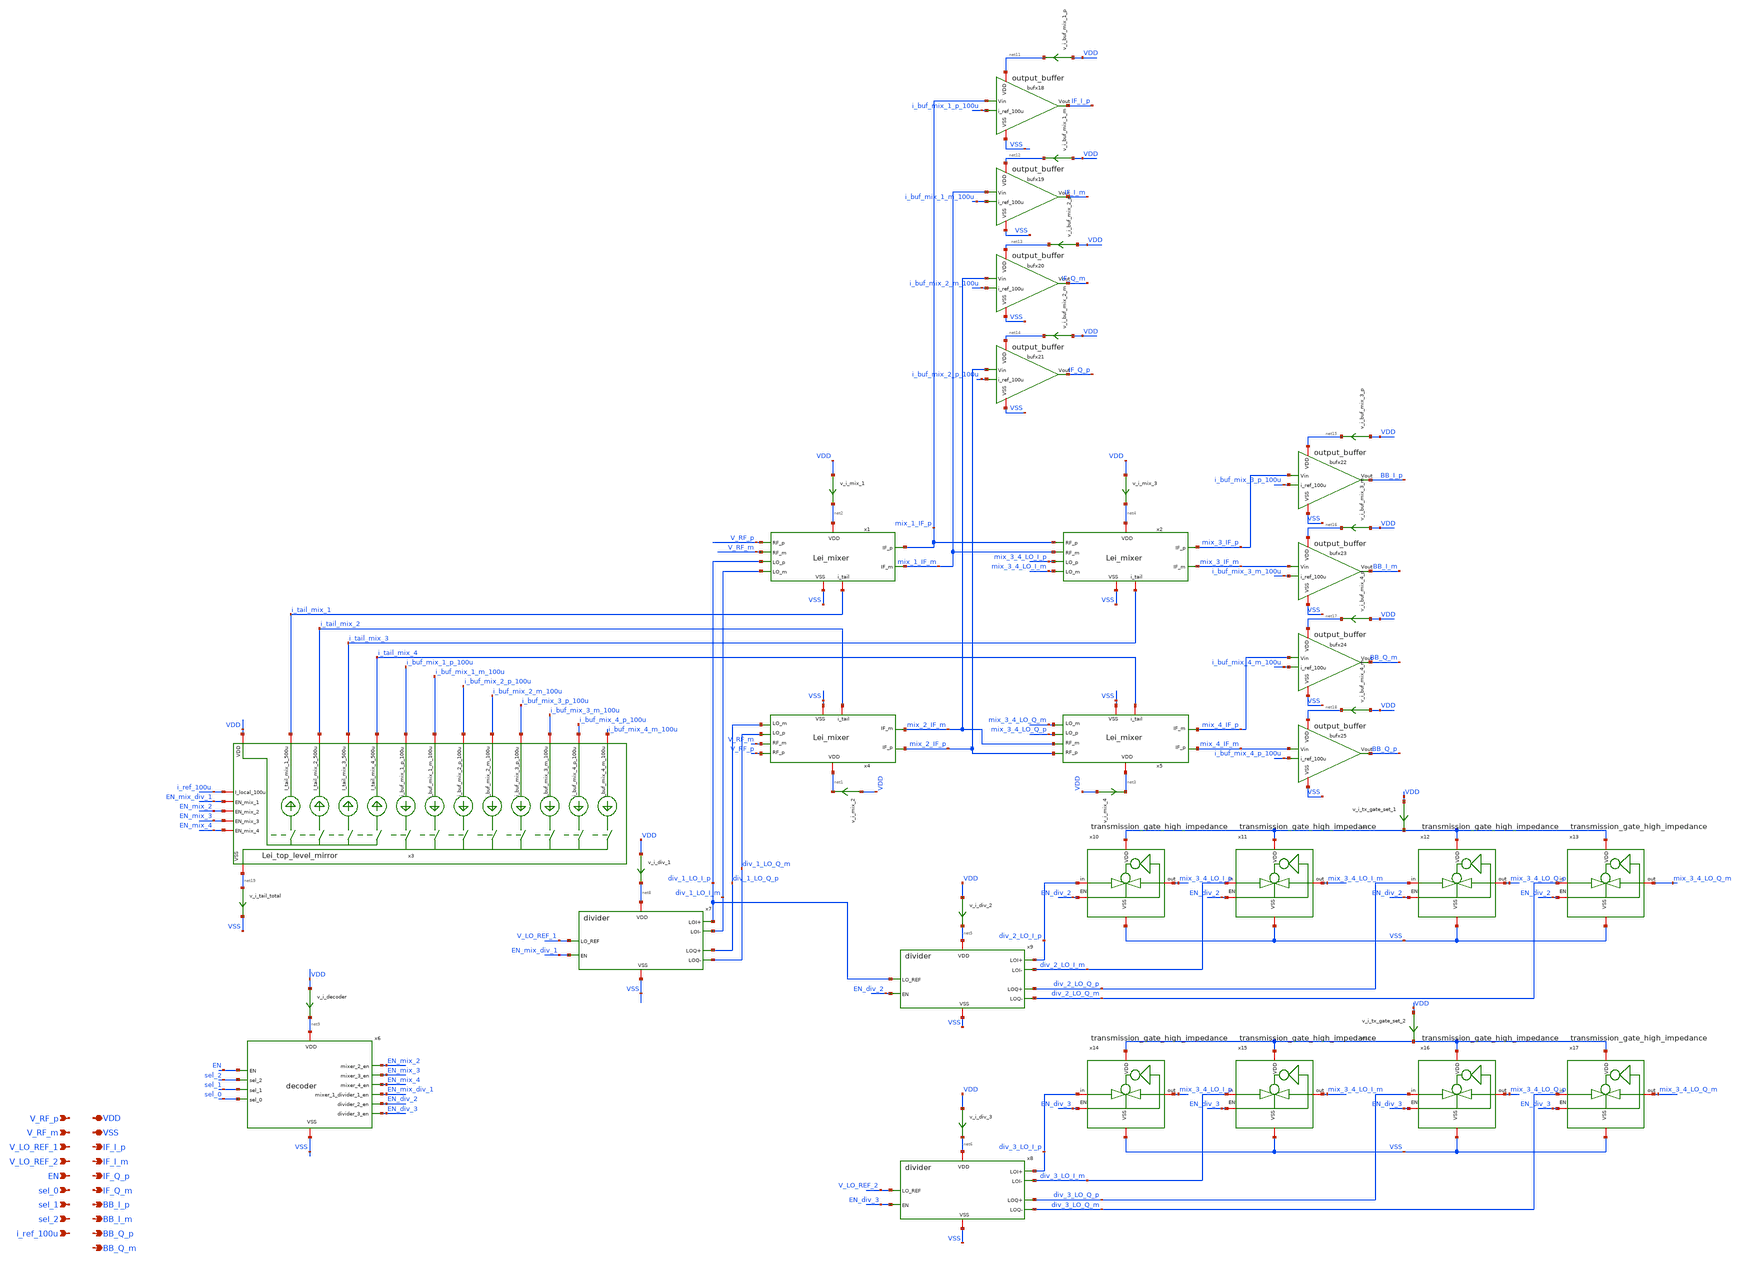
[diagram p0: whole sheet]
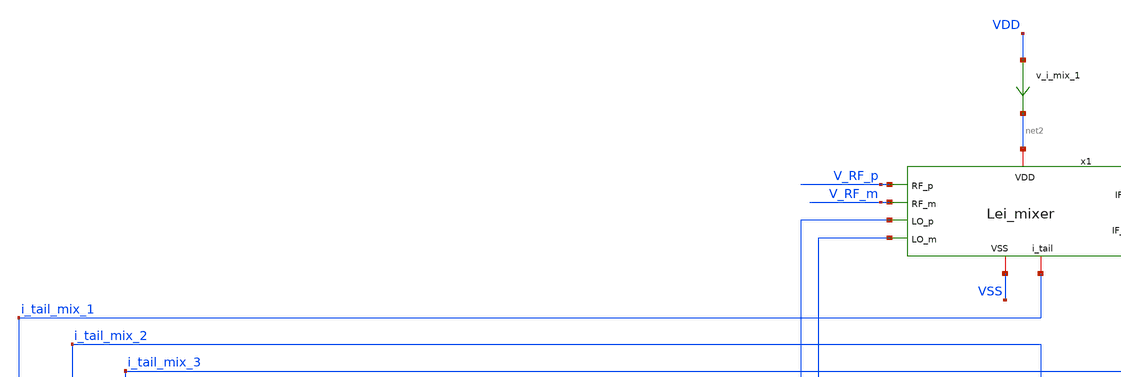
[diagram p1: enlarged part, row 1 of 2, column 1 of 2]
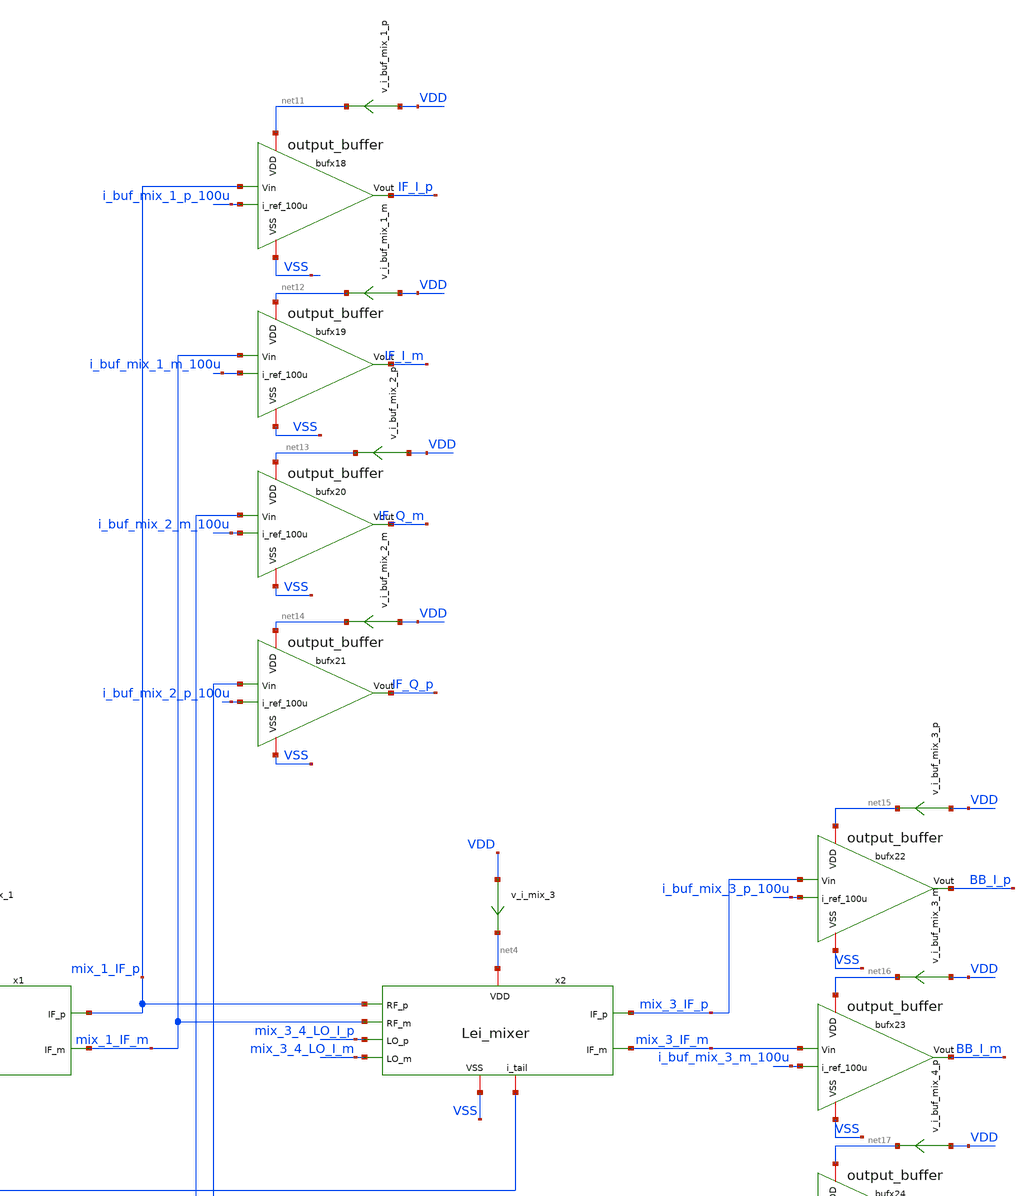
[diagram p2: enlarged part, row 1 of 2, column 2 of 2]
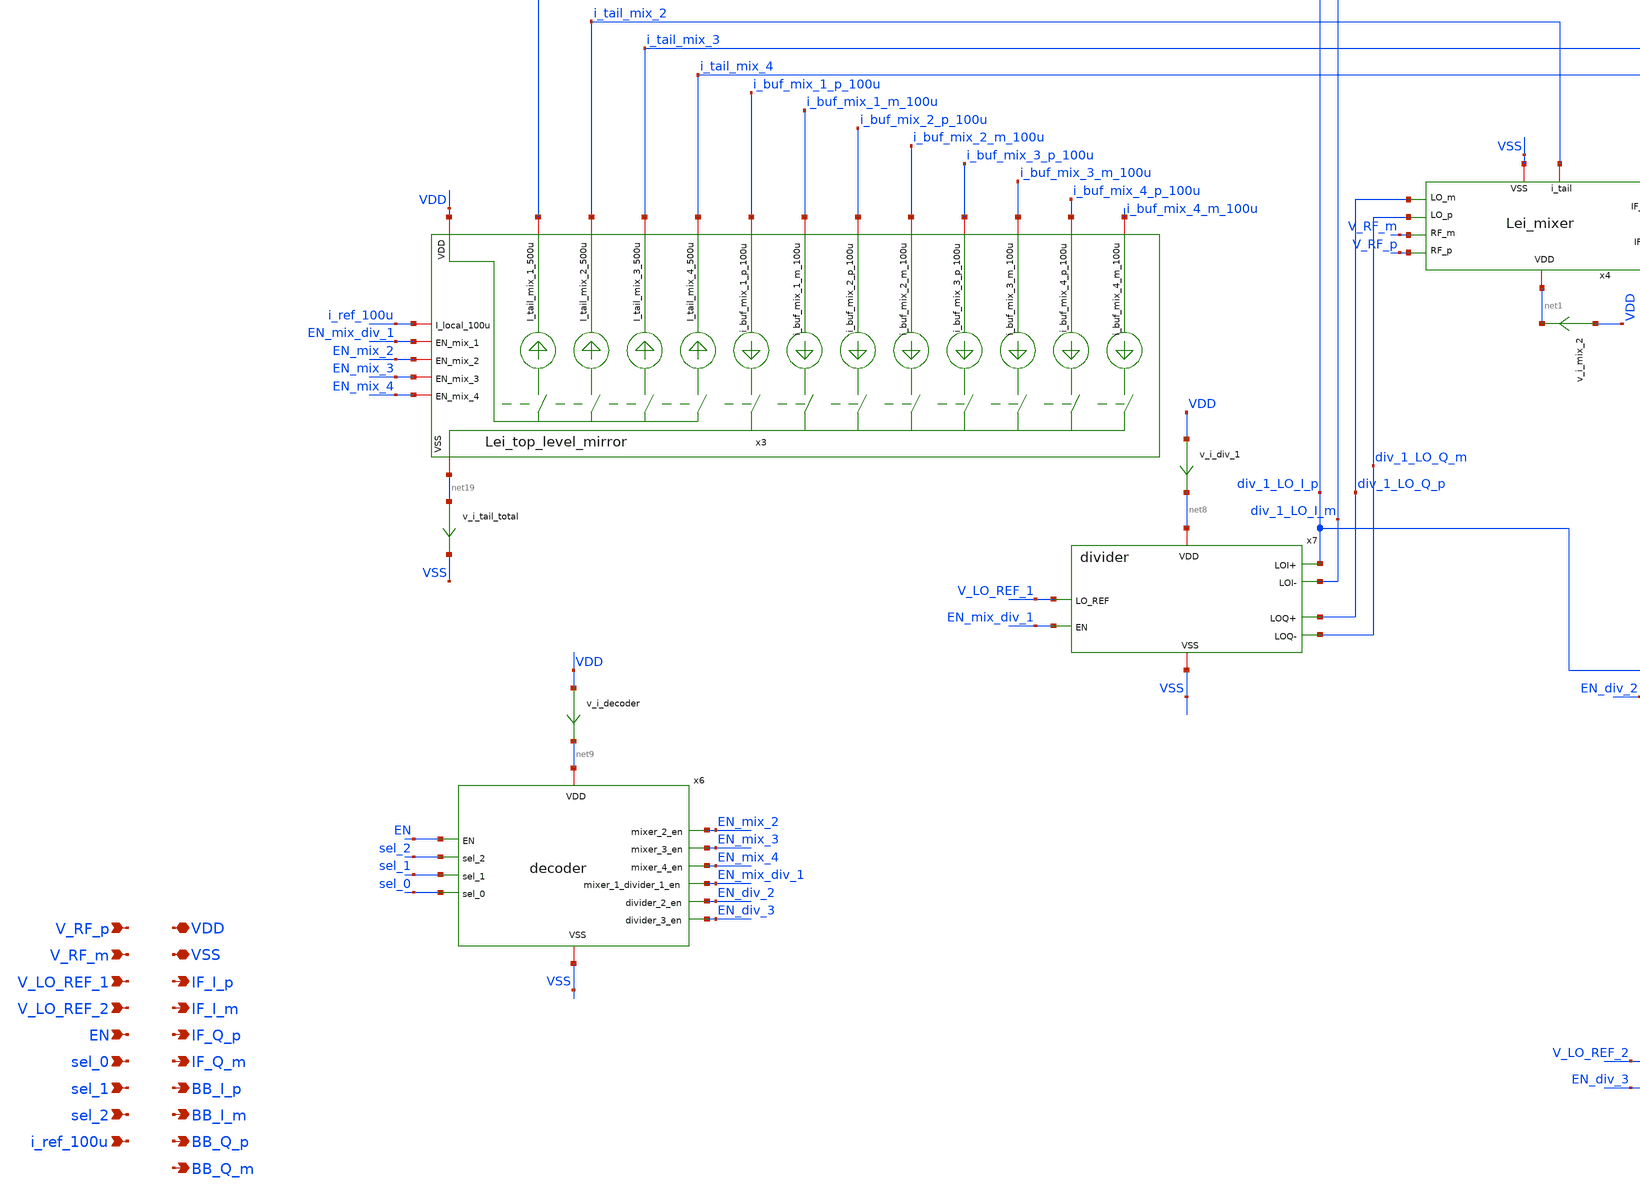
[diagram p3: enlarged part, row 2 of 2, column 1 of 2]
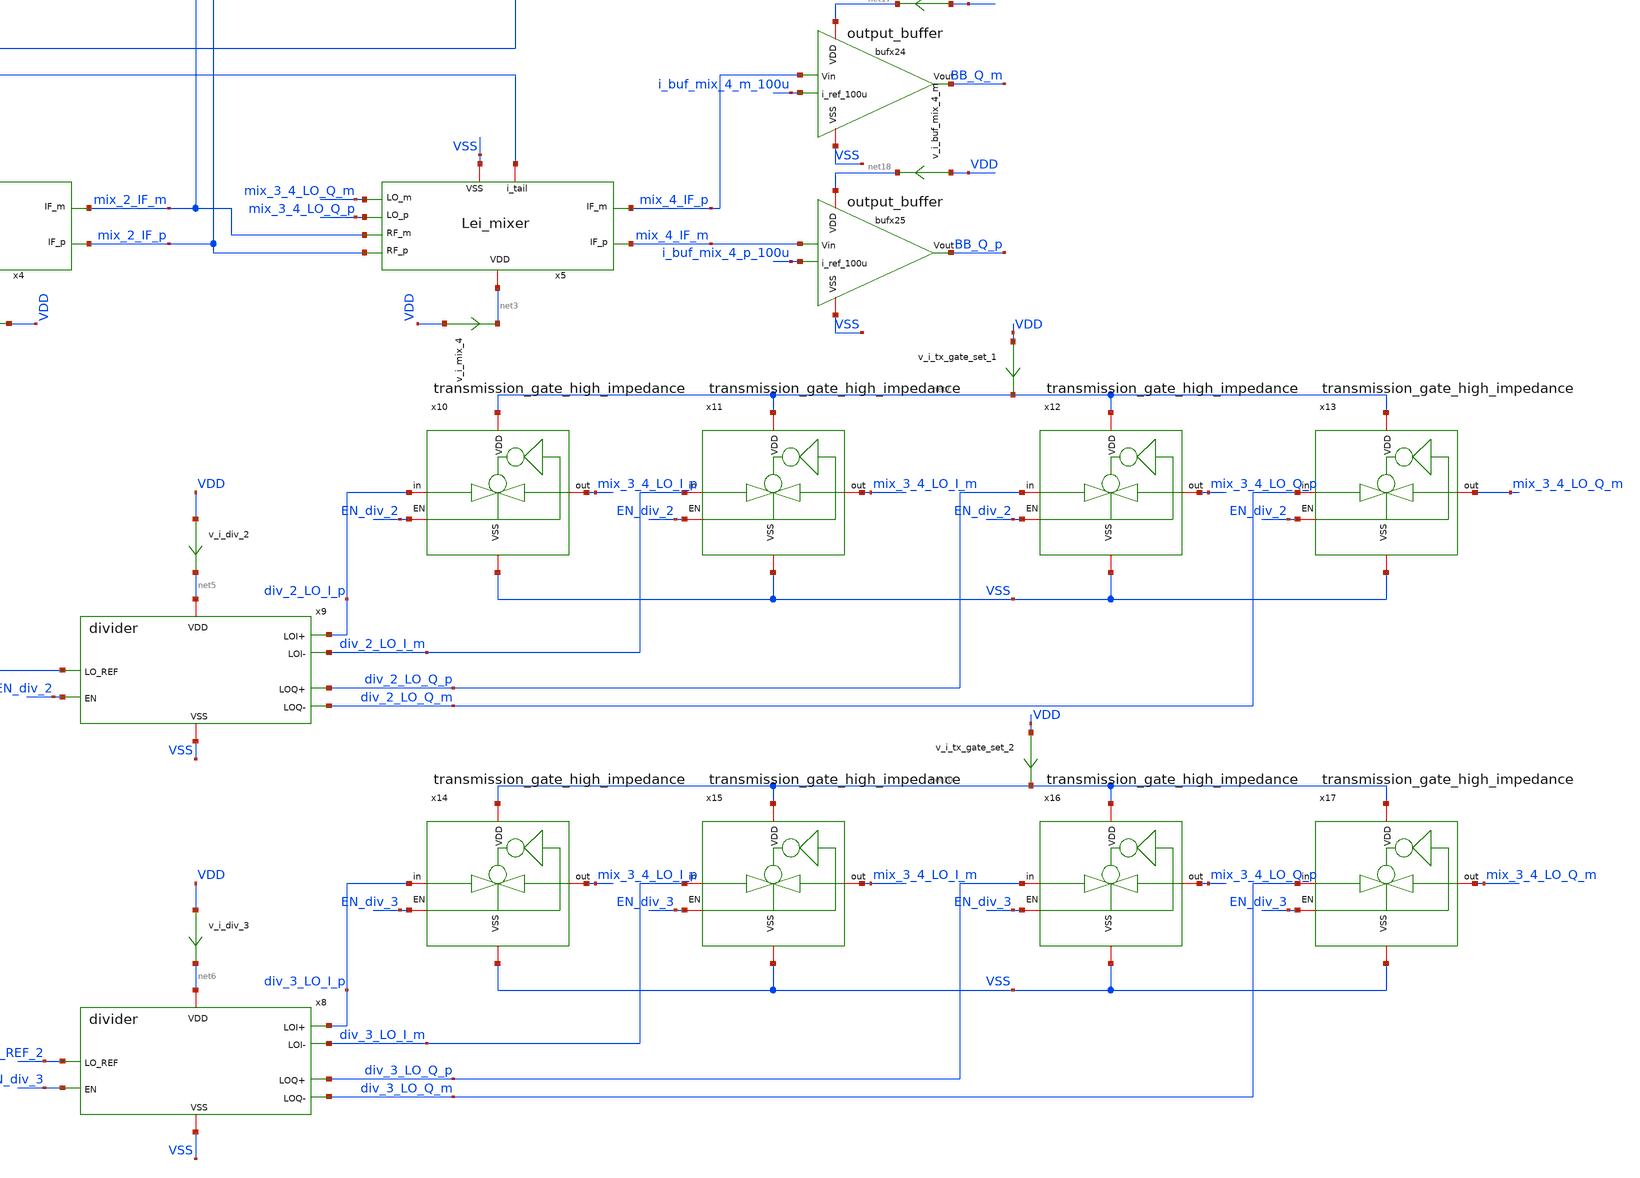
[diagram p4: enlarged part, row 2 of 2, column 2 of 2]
** sch_path: designs/top_level/schematic/top_pmos_mixer.sch
**.subckt top_pmos_mixer VDD VSS V_RF_p V_RF_m V_LO_REF_1 V_LO_REF_2 EN sel_0 sel_1 sel_2 i_ref_100u
*+ IF_I_p IF_I_m IF_Q_p IF_Q_m BB_I_p BB_I_m BB_Q_p BB_Q_m
*.iopin VDD
*.iopin VSS
*.ipin V_RF_p
*.ipin V_RF_m
*.ipin V_LO_REF_1
*.ipin V_LO_REF_2
*.ipin EN
*.ipin sel_0
*.ipin sel_1
*.ipin sel_2
*.ipin i_ref_100u
*.opin IF_I_p
*.opin IF_I_m
*.opin IF_Q_p
*.opin IF_Q_m
*.opin BB_I_p
*.opin BB_I_m
*.opin BB_Q_p
*.opin BB_Q_m
x6 net9 VSS EN sel_2 EN_mix_2 sel_1 EN_mix_3 EN_mix_4 sel_0 EN_div_2 EN_div_3 EN_mix_div_1 decoder
x7 net8 VSS V_LO_REF_1 div_1_LO_I_p div_1_LO_I_m div_1_LO_Q_p div_1_LO_Q_m EN_mix_div_1 divider
x8 net6 VSS V_LO_REF_2 div_3_LO_I_p div_3_LO_I_m div_3_LO_Q_p div_3_LO_Q_m EN_div_3 divider
x9 net5 VSS div_1_LO_I_p div_2_LO_I_p div_2_LO_I_m div_2_LO_Q_p div_2_LO_Q_m EN_div_2 divider
x10 net7 div_2_LO_I_p mix_3_4_LO_I_p VSS EN_div_2 transmission_gate_high_impedance
x11 net7 div_2_LO_I_m mix_3_4_LO_I_m VSS EN_div_2 transmission_gate_high_impedance
x12 net7 div_2_LO_Q_p mix_3_4_LO_Q_p VSS EN_div_2 transmission_gate_high_impedance
x13 net7 div_2_LO_Q_m mix_3_4_LO_Q_m VSS EN_div_2 transmission_gate_high_impedance
x14 net10 div_3_LO_I_p mix_3_4_LO_I_p VSS EN_div_3 transmission_gate_high_impedance
x15 net10 div_3_LO_I_m mix_3_4_LO_I_m VSS EN_div_3 transmission_gate_high_impedance
x16 net10 div_3_LO_Q_p mix_3_4_LO_Q_p VSS EN_div_3 transmission_gate_high_impedance
x17 net10 div_3_LO_Q_m mix_3_4_LO_Q_m VSS EN_div_3 transmission_gate_high_impedance
x18 IF_I_p mix_1_IF_p i_buf_mix_1_p_100u net11 VSS output_buffer
x19 IF_I_m mix_1_IF_m i_buf_mix_1_m_100u net12 VSS output_buffer
x20 IF_Q_m mix_2_IF_m i_buf_mix_2_m_100u net13 VSS output_buffer
x21 IF_Q_p mix_2_IF_p i_buf_mix_2_p_100u net14 VSS output_buffer
x22 BB_I_p mix_3_IF_p i_buf_mix_3_p_100u net15 VSS output_buffer
x23 BB_I_m mix_3_IF_m i_buf_mix_3_m_100u net16 VSS output_buffer
x24 BB_Q_m mix_4_IF_p i_buf_mix_4_m_100u net17 VSS output_buffer
x25 BB_Q_p mix_4_IF_m i_buf_mix_4_p_100u net18 VSS output_buffer
v_i_mix_1 VDD net2 0
.save i(v_i_mix_1)
v_i_mix_3 VDD net4 0
.save i(v_i_mix_3)
v_i_mix_4 VDD net3 0
.save i(v_i_mix_4)
v_i_mix_2 VDD net1 0
.save i(v_i_mix_2)
v_i_div_1 VDD net8 0
.save i(v_i_div_1)
v_i_div_2 VDD net5 0
.save i(v_i_div_2)
v_i_div_3 VDD net6 0
.save i(v_i_div_3)
v_i_tail_total net19 VSS 0
.save i(v_i_tail_total)
v_i_buf_mix_1_p VDD net11 0
.save i(v_i_buf_mix_1_p)
v_i_buf_mix_1_m VDD net12 0
.save i(v_i_buf_mix_1_m)
v_i_buf_mix_2_p VDD net13 0
.save i(v_i_buf_mix_2_p)
v_i_buf_mix_2_m VDD net14 0
.save i(v_i_buf_mix_2_m)
v_i_buf_mix_3_p VDD net15 0
.save i(v_i_buf_mix_3_p)
v_i_buf_mix_3_m VDD net16 0
.save i(v_i_buf_mix_3_m)
v_i_buf_mix_4_p VDD net17 0
.save i(v_i_buf_mix_4_p)
v_i_buf_mix_4_m VDD net18 0
.save i(v_i_buf_mix_4_m)
v_i_decoder VDD net9 0
.save i(v_i_decoder)
v_i_tx_gate_set_1 VDD net7 0
.save i(v_i_tx_gate_set_1)
v_i_tx_gate_set_2 VDD net10 0
.save i(v_i_tx_gate_set_2)
x3 VDD i_tail_mix_1 EN_mix_div_1 EN_mix_2 EN_mix_3 EN_mix_4 i_tail_mix_2 i_tail_mix_3 i_ref_100u
+ i_tail_mix_4 net19 i_buf_mix_1_p_100u i_buf_mix_1_m_100u i_buf_mix_2_p_100u i_buf_mix_2_m_100u
+ i_buf_mix_3_p_100u i_buf_mix_3_m_100u i_buf_mix_4_p_100u i_buf_mix_4_m_100u Lei_top_level_mirror
x1 mix_1_IF_p V_RF_p net2 VSS mix_1_IF_m V_RF_m div_1_LO_I_p i_tail_mix_1 div_1_LO_I_m Lei_mixer
x2 mix_3_IF_p mix_1_IF_p net4 VSS mix_3_IF_m mix_1_IF_m mix_3_4_LO_I_p i_tail_mix_3 mix_3_4_LO_I_m
+ Lei_mixer
x4 mix_2_IF_p V_RF_p net1 VSS mix_2_IF_m V_RF_m div_1_LO_Q_m i_tail_mix_2 div_1_LO_Q_p Lei_mixer
x5 mix_4_IF_m mix_2_IF_p net3 VSS mix_4_IF_p mix_2_IF_m mix_3_4_LO_Q_p i_tail_mix_4 mix_3_4_LO_Q_m
+ Lei_mixer
**.ends
.end
